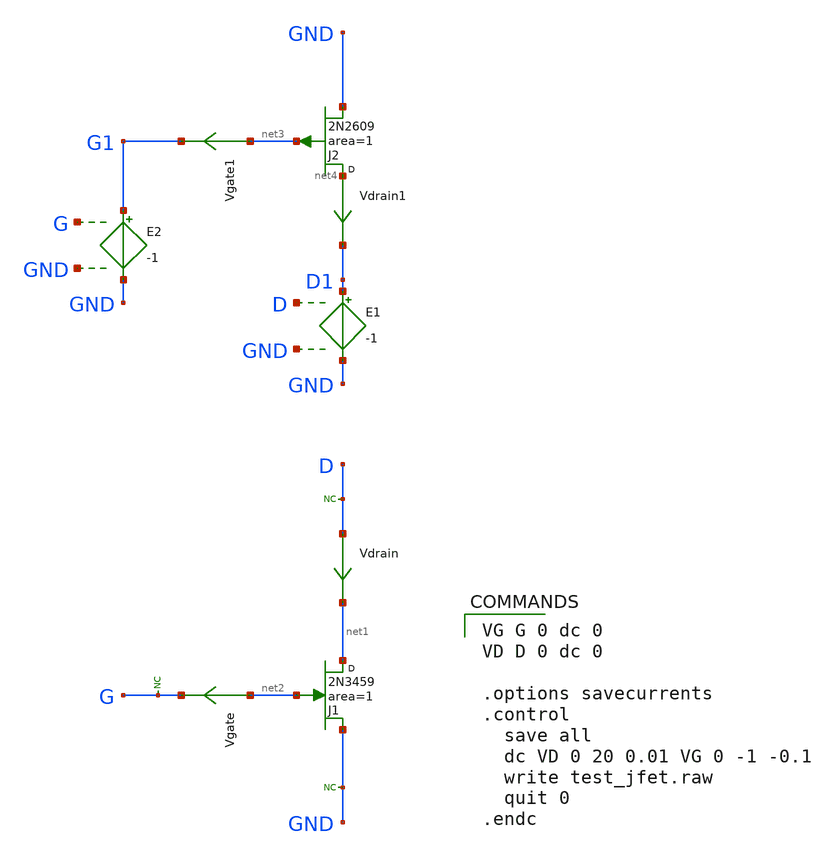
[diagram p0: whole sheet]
** sch_path: xschem_libraries_oa/examples/test_jfet/schematic/test_jfet.sch
* Copyright (C) 1998-2024 Stefan Frederik Schippers
* This program is free software; you can redistribute it and/or modify
* it under the terms of the GNU General Public License as published by
* the Free Software Foundation; either version 2 of the License, or
* (at your option) any later version.
* This program is distributed in the hope that it will be useful,
* but WITHOUT ANY WARRANTY; without even the implied warranty of
* MERCHANTABILITY or FITNESS FOR A PARTICULAR PURPOSE.  See the
* GNU General Public License for more details.
* You should have received a copy of the GNU General Public License
* along with this program; if not, write to the Free Software
**.subckt test_jfet
J1 net1 net2 GND 2N3459 area=1 m=1
* noconn GND
* noconn D
* noconn G
Vgate net2 G 0
.save i(vgate)
Vdrain D net1 0
.save i(vdrain)
J2 net4 net3 GND 2N2609 area=1 m=1
Vgate1 net3 G1 0
.save i(vgate1)
Vdrain1 net4 D1 0
.save i(vdrain1)
E1 D1 GND D GND -1
E2 G1 GND G GND -1
**** begin user architecture code

VG G 0 dc 0
VD D 0 dc 0

.options savecurrents
.control
  save all
  dc VD 0 20 0.01 VG 0 -1 -0.1
  write test_jfet.raw
  quit 0
.endc



.MODEL 2N3459 NJF(VTO=-1.4 BETA=1.265m BETATCE=-0.5 LAMBDA=4m RD=1 RS=1 CGS=2.916p CGD=2.8p PB=0.5
+ IS=114.5f XTI=3 AF=1 FC=0.5 N=1 NR=2)
.model 2N2609 PJF (Beta=3.2m Betatce=-500m Rd=1 Rs=1 Lambda=18.5m Vto=-1.408 Vtotc=-2.5m Is=461.5f
+ Isr=4.402p N=1 Nr=2 Xti=3 Alpha=32.54u Vk=393.2 Cgd=6.5p M=278.9m Pb=1 Fc=500m Cgs=9p Kf=0.2062f Af=1)

**** end user architecture code
**.ends
.end
